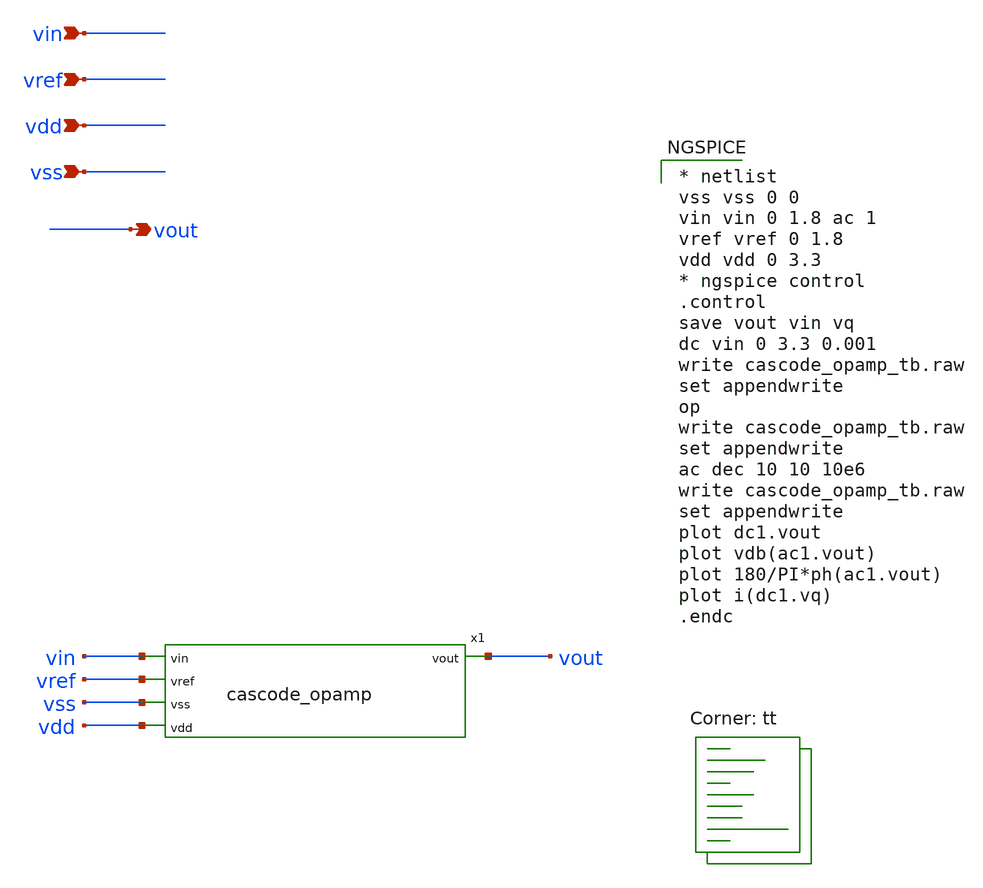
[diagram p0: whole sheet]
** sch_path: xschem/cascode_opamp_tb.sch
**.subckt cascode_opamp_tb vss vout vdd vref vin
*.ipin vss
*.opin vout
*.ipin vdd
*.ipin vref
*.ipin vin
x1 vout vin vref vss vdd cascode_opamp
**** begin user architecture code

* netlist
vss vss 0 0
vin vin 0 1.8 ac 1
vref vref 0 1.8
vdd vdd 0 3.3
* ngspice control
.control
save vout vin vq
dc vin 0 3.3 0.001
write cascode_opamp_tb.raw
set appendwrite
op
write cascode_opamp_tb.raw
set appendwrite
ac dec 10 10 10e6
write cascode_opamp_tb.raw
set appendwrite
plot dc1.vout
plot vdb(ac1.vout)
plot 180/PI*ph(ac1.vout)
plot i(dc1.vq)
.endc


.lib $::SKYWATER_MODELS/sky130.lib.spice tt
**** end user architecture code
**.ends

* expanding   symbol:  cascode_opamp.sym # of pins=5
** sym_path: xschem/cascode_opamp.sym
** sch_path: xschem/cascode_opamp.sch
.subckt cascode_opamp vout vin vref vss vdd
*.ipin vin
*.ipin vref
*.ipin vss
*.opin vout
*.ipin vdd
I0 vdd net2 600n
XM1 net1 net1 vss vss sky130_fd_pr__nfet_g5v0d10v5 L=0.5 W=1 nf=1 ad='int((nf+1)/2) * W/nf * 0.29' as='int((nf+2)/2) * W/nf * 0.29'
+ pd='2*int((nf+1)/2) * (W/nf + 0.29)' ps='2*int((nf+2)/2) * (W/nf + 0.29)' nrd='0.29 / W' nrs='0.29 / W'
+ sa=0 sb=0 sd=0 mult=1 m=1
XM2 net2 net2 net1 vss sky130_fd_pr__nfet_g5v0d10v5 L=0.5 W=1 nf=1 ad='int((nf+1)/2) * W/nf * 0.29' as='int((nf+2)/2) * W/nf * 0.29'
+ pd='2*int((nf+1)/2) * (W/nf + 0.29)' ps='2*int((nf+2)/2) * (W/nf + 0.29)' nrd='0.29 / W' nrs='0.29 / W'
+ sa=0 sb=0 sd=0 mult=1 m=1
XM3 net3 net1 vss vss sky130_fd_pr__nfet_g5v0d10v5 L=0.5 W=1 nf=1 ad='int((nf+1)/2) * W/nf * 0.29' as='int((nf+2)/2) * W/nf * 0.29'
+ pd='2*int((nf+1)/2) * (W/nf + 0.29)' ps='2*int((nf+2)/2) * (W/nf + 0.29)' nrd='0.29 / W' nrs='0.29 / W'
+ sa=0 sb=0 sd=0 mult=1 m=1
XM4 vp net2 net3 vss sky130_fd_pr__nfet_g5v0d10v5 L=0.5 W=1 nf=1 ad='int((nf+1)/2) * W/nf * 0.29' as='int((nf+2)/2) * W/nf * 0.29'
+ pd='2*int((nf+1)/2) * (W/nf + 0.29)' ps='2*int((nf+2)/2) * (W/nf + 0.29)' nrd='0.29 / W' nrs='0.29 / W'
+ sa=0 sb=0 sd=0 mult=1 m=1
XM5 net5 vref net4 vss sky130_fd_pr__nfet_g5v0d10v5 L=0.5 W=1 nf=1 ad='int((nf+1)/2) * W/nf * 0.29' as='int((nf+2)/2) * W/nf * 0.29'
+ pd='2*int((nf+1)/2) * (W/nf + 0.29)' ps='2*int((nf+2)/2) * (W/nf + 0.29)' nrd='0.29 / W' nrs='0.29 / W'
+ sa=0 sb=0 sd=0 mult=1 m=1
XM6 vx vin net4 vss sky130_fd_pr__nfet_g5v0d10v5 L=0.5 W=1 nf=1 ad='int((nf+1)/2) * W/nf * 0.29' as='int((nf+2)/2) * W/nf * 0.29'
+ pd='2*int((nf+1)/2) * (W/nf + 0.29)' ps='2*int((nf+2)/2) * (W/nf + 0.29)' nrd='0.29 / W' nrs='0.29 / W'
+ sa=0 sb=0 sd=0 mult=1 m=1
XM7 vb2 vb1 net5 vss sky130_fd_pr__nfet_g5v0d10v5 L=0.5 W=1 nf=1 ad='int((nf+1)/2) * W/nf * 0.29' as='int((nf+2)/2) * W/nf * 0.29'
+ pd='2*int((nf+1)/2) * (W/nf + 0.29)' ps='2*int((nf+2)/2) * (W/nf + 0.29)' nrd='0.29 / W' nrs='0.29 / W'
+ sa=0 sb=0 sd=0 mult=1 m=1
XM8 vout vb1 vx vss sky130_fd_pr__nfet_g5v0d10v5 L=0.5 W=1 nf=1 ad='int((nf+1)/2) * W/nf * 0.29' as='int((nf+2)/2) * W/nf * 0.29'
+ pd='2*int((nf+1)/2) * (W/nf + 0.29)' ps='2*int((nf+2)/2) * (W/nf + 0.29)' nrd='0.29 / W' nrs='0.29 / W'
+ sa=0 sb=0 sd=0 mult=1 m=1
XM9 vb2 vb2 vb3 vdd sky130_fd_pr__pfet_g5v0d10v5 L=0.5 W=1 nf=1 ad='int((nf+1)/2) * W/nf * 0.29' as='int((nf+2)/2) * W/nf * 0.29'
+ pd='2*int((nf+1)/2) * (W/nf + 0.29)' ps='2*int((nf+2)/2) * (W/nf + 0.29)' nrd='0.29 / W' nrs='0.29 / W'
+ sa=0 sb=0 sd=0 mult=1 m=1
XM10 vout vb2 vy vdd sky130_fd_pr__pfet_g5v0d10v5 L=0.5 W=1 nf=1 ad='int((nf+1)/2) * W/nf * 0.29' as='int((nf+2)/2) * W/nf * 0.29'
+ pd='2*int((nf+1)/2) * (W/nf + 0.29)' ps='2*int((nf+2)/2) * (W/nf + 0.29)' nrd='0.29 / W' nrs='0.29 / W'
+ sa=0 sb=0 sd=0 mult=1 m=1
XM11 vb3 vb3 vdd vdd sky130_fd_pr__pfet_g5v0d10v5 L=0.5 W=1 nf=1 ad='int((nf+1)/2) * W/nf * 0.29' as='int((nf+2)/2) * W/nf * 0.29'
+ pd='2*int((nf+1)/2) * (W/nf + 0.29)' ps='2*int((nf+2)/2) * (W/nf + 0.29)' nrd='0.29 / W' nrs='0.29 / W'
+ sa=0 sb=0 sd=0 mult=1 m=1
XM12 vy vb3 vdd vdd sky130_fd_pr__pfet_g5v0d10v5 L=0.5 W=1 nf=1 ad='int((nf+1)/2) * W/nf * 0.29' as='int((nf+2)/2) * W/nf * 0.29'
+ pd='2*int((nf+1)/2) * (W/nf + 0.29)' ps='2*int((nf+2)/2) * (W/nf + 0.29)' nrd='0.29 / W' nrs='0.29 / W'
+ sa=0 sb=0 sd=0 mult=1 m=1
Vbias net4 vp 0
.save i(vbias)
V1 vb1 vss 2
.ends

.end
